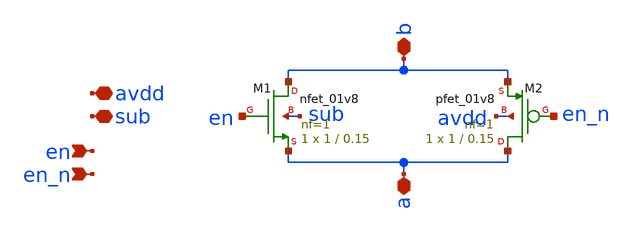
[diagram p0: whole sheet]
** sch_path: test/design/tg.sch
**.subckt tg avdd sub en en_n a b
*.iopin avdd
*.iopin sub
*.ipin en
*.ipin en_n
*.iopin a
*.iopin b
XM1 b en a sub sky130_fd_pr__nfet_01v8 L=0.15 W=1 nf=1 ad='int((nf+1)/2) * W/nf * 0.29' as='int((nf+2)/2) * W/nf * 0.29'
+ pd='2*int((nf+1)/2) * (W/nf + 0.29)' ps='2*int((nf+2)/2) * (W/nf + 0.29)' nrd='0.29 / W' nrs='0.29 / W'
+ sa=0 sb=0 sd=0 mult=1 m=1
XM2 a en_n b avdd sky130_fd_pr__pfet_01v8 L=0.15 W=1 nf=1 ad='int((nf+1)/2) * W/nf * 0.29' as='int((nf+2)/2) * W/nf * 0.29'
+ pd='2*int((nf+1)/2) * (W/nf + 0.29)' ps='2*int((nf+2)/2) * (W/nf + 0.29)' nrd='0.29 / W' nrs='0.29 / W'
+ sa=0 sb=0 sd=0 mult=1 m=1
**.ends
.end
